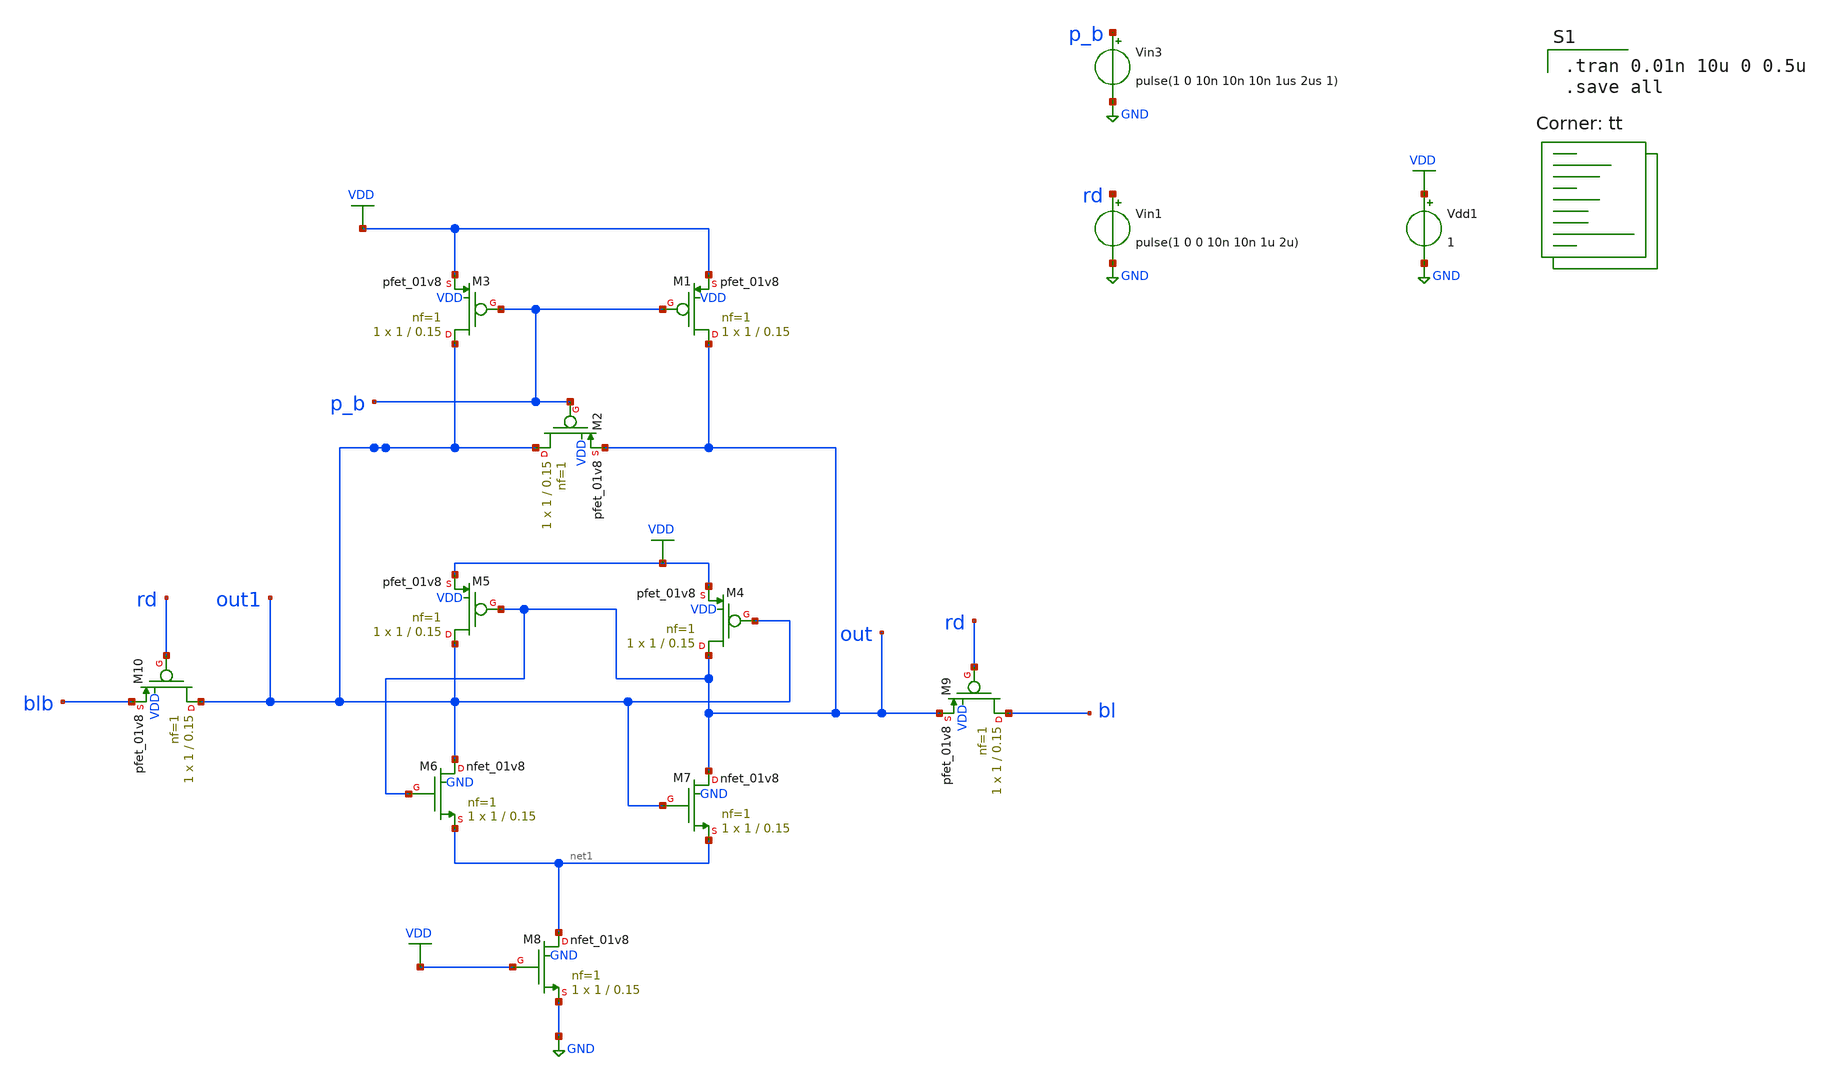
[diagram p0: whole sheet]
** sch_path: gates/Memory/Sense amplifier sim.sch
**.subckt Sense amplifier sim
XM1 out p_b VDD VDD sky130_fd_pr__pfet_01v8 L=0.15 W=1 nf=1 ad='int((nf+1)/2) * W/nf * 0.29' as='int((nf+2)/2) * W/nf * 0.29'
+ pd='2*int((nf+1)/2) * (W/nf + 0.29)' ps='2*int((nf+2)/2) * (W/nf + 0.29)' nrd='0.29 / W' nrs='0.29 / W'
+ sa=0 sb=0 sd=0 mult=1 m=1
XM2 out1 p_b out VDD sky130_fd_pr__pfet_01v8 L=0.15 W=1 nf=1 ad='int((nf+1)/2) * W/nf * 0.29' as='int((nf+2)/2) * W/nf * 0.29'
+ pd='2*int((nf+1)/2) * (W/nf + 0.29)' ps='2*int((nf+2)/2) * (W/nf + 0.29)' nrd='0.29 / W' nrs='0.29 / W'
+ sa=0 sb=0 sd=0 mult=1 m=1
XM3 out1 p_b VDD VDD sky130_fd_pr__pfet_01v8 L=0.15 W=1 nf=1 ad='int((nf+1)/2) * W/nf * 0.29' as='int((nf+2)/2) * W/nf * 0.29'
+ pd='2*int((nf+1)/2) * (W/nf + 0.29)' ps='2*int((nf+2)/2) * (W/nf + 0.29)' nrd='0.29 / W' nrs='0.29 / W'
+ sa=0 sb=0 sd=0 mult=1 m=1
XM4 out out1 VDD VDD sky130_fd_pr__pfet_01v8 L=0.15 W=1 nf=1 ad='int((nf+1)/2) * W/nf * 0.29' as='int((nf+2)/2) * W/nf * 0.29'
+ pd='2*int((nf+1)/2) * (W/nf + 0.29)' ps='2*int((nf+2)/2) * (W/nf + 0.29)' nrd='0.29 / W' nrs='0.29 / W'
+ sa=0 sb=0 sd=0 mult=1 m=1
XM5 out1 out VDD VDD sky130_fd_pr__pfet_01v8 L=0.15 W=1 nf=1 ad='int((nf+1)/2) * W/nf * 0.29' as='int((nf+2)/2) * W/nf * 0.29'
+ pd='2*int((nf+1)/2) * (W/nf + 0.29)' ps='2*int((nf+2)/2) * (W/nf + 0.29)' nrd='0.29 / W' nrs='0.29 / W'
+ sa=0 sb=0 sd=0 mult=1 m=1
XM6 out1 out net1 GND sky130_fd_pr__nfet_01v8 L=0.15 W=1 nf=1 ad='int((nf+1)/2) * W/nf * 0.29' as='int((nf+2)/2) * W/nf * 0.29'
+ pd='2*int((nf+1)/2) * (W/nf + 0.29)' ps='2*int((nf+2)/2) * (W/nf + 0.29)' nrd='0.29 / W' nrs='0.29 / W'
+ sa=0 sb=0 sd=0 mult=1 m=1
XM7 out out1 net1 GND sky130_fd_pr__nfet_01v8 L=0.15 W=1 nf=1 ad='int((nf+1)/2) * W/nf * 0.29' as='int((nf+2)/2) * W/nf * 0.29'
+ pd='2*int((nf+1)/2) * (W/nf + 0.29)' ps='2*int((nf+2)/2) * (W/nf + 0.29)' nrd='0.29 / W' nrs='0.29 / W'
+ sa=0 sb=0 sd=0 mult=1 m=1
XM8 net1 VDD GND GND sky130_fd_pr__nfet_01v8 L=0.15 W=1 nf=1 ad='int((nf+1)/2) * W/nf * 0.29' as='int((nf+2)/2) * W/nf * 0.29'
+ pd='2*int((nf+1)/2) * (W/nf + 0.29)' ps='2*int((nf+2)/2) * (W/nf + 0.29)' nrd='0.29 / W' nrs='0.29 / W'
+ sa=0 sb=0 sd=0 mult=1 m=1
Vdd1 VDD GND 1
Vin1 rd GND pulse(1 0 0 10n 10n 1u 2u)
XM9 bl rd out VDD sky130_fd_pr__pfet_01v8 L=0.15 W=1 nf=1 ad='int((nf+1)/2) * W/nf * 0.29' as='int((nf+2)/2) * W/nf * 0.29'
+ pd='2*int((nf+1)/2) * (W/nf + 0.29)' ps='2*int((nf+2)/2) * (W/nf + 0.29)' nrd='0.29 / W' nrs='0.29 / W'
+ sa=0 sb=0 sd=0 mult=1 m=1
XM10 out1 rd blb VDD sky130_fd_pr__pfet_01v8 L=0.15 W=1 nf=1 ad='int((nf+1)/2) * W/nf * 0.29' as='int((nf+2)/2) * W/nf * 0.29'
+ pd='2*int((nf+1)/2) * (W/nf + 0.29)' ps='2*int((nf+2)/2) * (W/nf + 0.29)' nrd='0.29 / W' nrs='0.29 / W'
+ sa=0 sb=0 sd=0 mult=1 m=1
Vin3 p_b GND pulse(1 0 10n 10n 10n 1us 2us 1)
**** begin user architecture code

.tran 0.01n 10u 0 0.5u
.save all

.lib $::SKYWATER_MODELS/sky130.lib.spice tt
**** end user architecture code
**.ends
.GLOBAL VDD
.GLOBAL GND
.end
